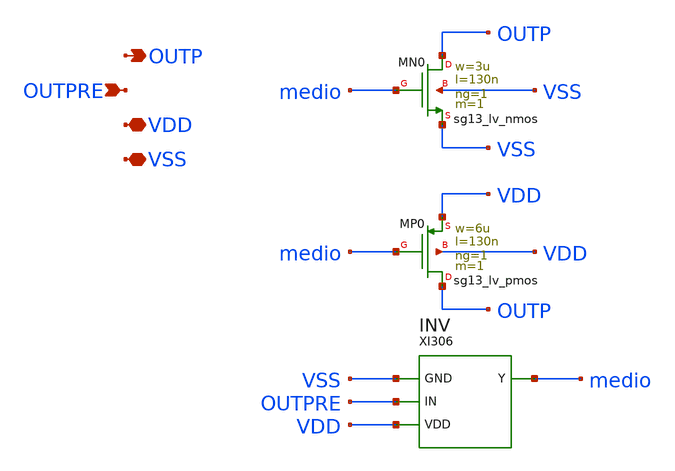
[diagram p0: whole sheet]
** sch_path: SoC6169-main/schematic/xschem/BUFFER.sch
* Copyright 2026 USFQ CAM team
* Licensed under the Apache License, Version 2.0 (the "License");
* you may not use this file except in compliance with the License.
* You may obtain a copy of the License at
* https://www.apache.org/licenses/LICENSE-2.0
* Unless required by applicable law or agreed to in writing, software
* distributed under the License is distributed on an "AS IS" BASIS,
* WITHOUT WARRANTIES OR CONDITIONS OF ANY KIND, either express or implied.
* See the License for the specific language governing permissions and
* limitations under the License.
**.subckt BUFFER OUTP OUTPRE VDD VSS
*.opin OUTP
*.ipin OUTPRE
*.iopin VDD
*.iopin VSS
XMN0 OUTP medio VSS VSS sg13_lv_nmos w=3u l=130n ng=1 m=1 mm_ok=1
XMP0 OUTP medio VDD VDD sg13_lv_pmos w=6u l=130n ng=1 m=1 mm_ok=1
XI306 VSS OUTPRE VDD medio INV
**.ends

* expanding   symbol:  INV.sym # of pins=4
** sym_path: SoC6169-main/schematic/xschem/INV.sym
** sch_path: SoC6169-main/schematic/xschem/INV.sch
.subckt INV GND IN VDD Y
*.iopin GND
*.ipin IN
*.iopin VDD
*.opin Y
XMN0 Y IN GND GND sg13_lv_nmos w=200n l=130n ng=1 m=1 mm_ok=1
XMP0 Y IN VDD VDD sg13_lv_pmos w=400n l=130n ng=1 m=1 mm_ok=1
.ends

.end
